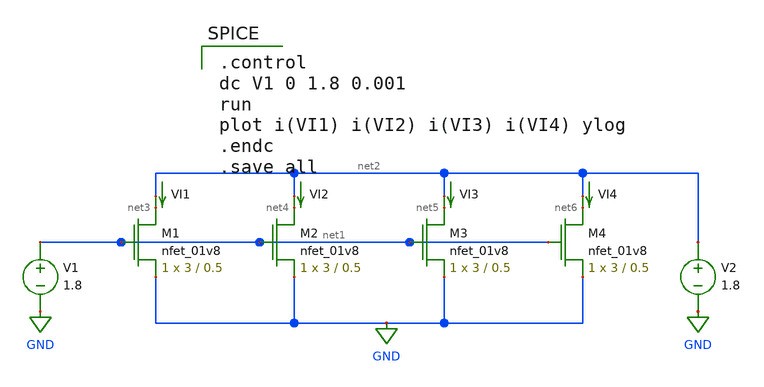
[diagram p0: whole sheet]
** sch_path: mctest/nmosmctest.sch
**.subckt nmosmctest
XM1 net3 net1 GND GND sky130_fd_pr__nfet_01v8 L=0.5 W=3 nf=1 ad='int((nf+1)/2) * W/nf * 0.29' as='int((nf+2)/2) * W/nf * 0.29'
+ pd='2*int((nf+1)/2) * (W/nf + 0.29)' ps='2*int((nf+2)/2) * (W/nf + 0.29)' nrd='0.29 / W' nrs='0.29 / W'
+ sa=0 sb=0 sd=0 mult=1 m=1
XM2 net4 net1 GND GND sky130_fd_pr__nfet_01v8 L=0.5 W=3 nf=1 ad='int((nf+1)/2) * W/nf * 0.29' as='int((nf+2)/2) * W/nf * 0.29'
+ pd='2*int((nf+1)/2) * (W/nf + 0.29)' ps='2*int((nf+2)/2) * (W/nf + 0.29)' nrd='0.29 / W' nrs='0.29 / W'
+ sa=0 sb=0 sd=0 mult=1 m=1
XM3 net5 net1 GND GND sky130_fd_pr__nfet_01v8 L=0.5 W=3 nf=1 ad='int((nf+1)/2) * W/nf * 0.29' as='int((nf+2)/2) * W/nf * 0.29'
+ pd='2*int((nf+1)/2) * (W/nf + 0.29)' ps='2*int((nf+2)/2) * (W/nf + 0.29)' nrd='0.29 / W' nrs='0.29 / W'
+ sa=0 sb=0 sd=0 mult=1 m=1
XM4 net6 net1 GND GND sky130_fd_pr__nfet_01v8 L=0.5 W=3 nf=1 ad='int((nf+1)/2) * W/nf * 0.29' as='int((nf+2)/2) * W/nf * 0.29'
+ pd='2*int((nf+1)/2) * (W/nf + 0.29)' ps='2*int((nf+2)/2) * (W/nf + 0.29)' nrd='0.29 / W' nrs='0.29 / W'
+ sa=0 sb=0 sd=0 mult=1 m=1
V1 net1 GND 1.8
V2 net2 GND 1.8
VI1 net2 net3 0
.save i(vi1)
VI2 net2 net4 0
.save i(vi2)
VI3 net2 net5 0
.save i(vi3)
VI4 net2 net6 0
.save i(vi4)
**** begin user architecture code

.option wnflag=1
.param MC_SWITCH=1.0
.lib ~/skywater/skywater-pdk/libraries/sky130_fd_pr_ngspice/latest/models/sky130.lib.spice tt


.control
dc V1 0 1.8 0.001
run
plot i(VI1) i(VI2) i(VI3) i(VI4) ylog
.endc
.save all

**** end user architecture code
**.ends
.GLOBAL GND
.end
